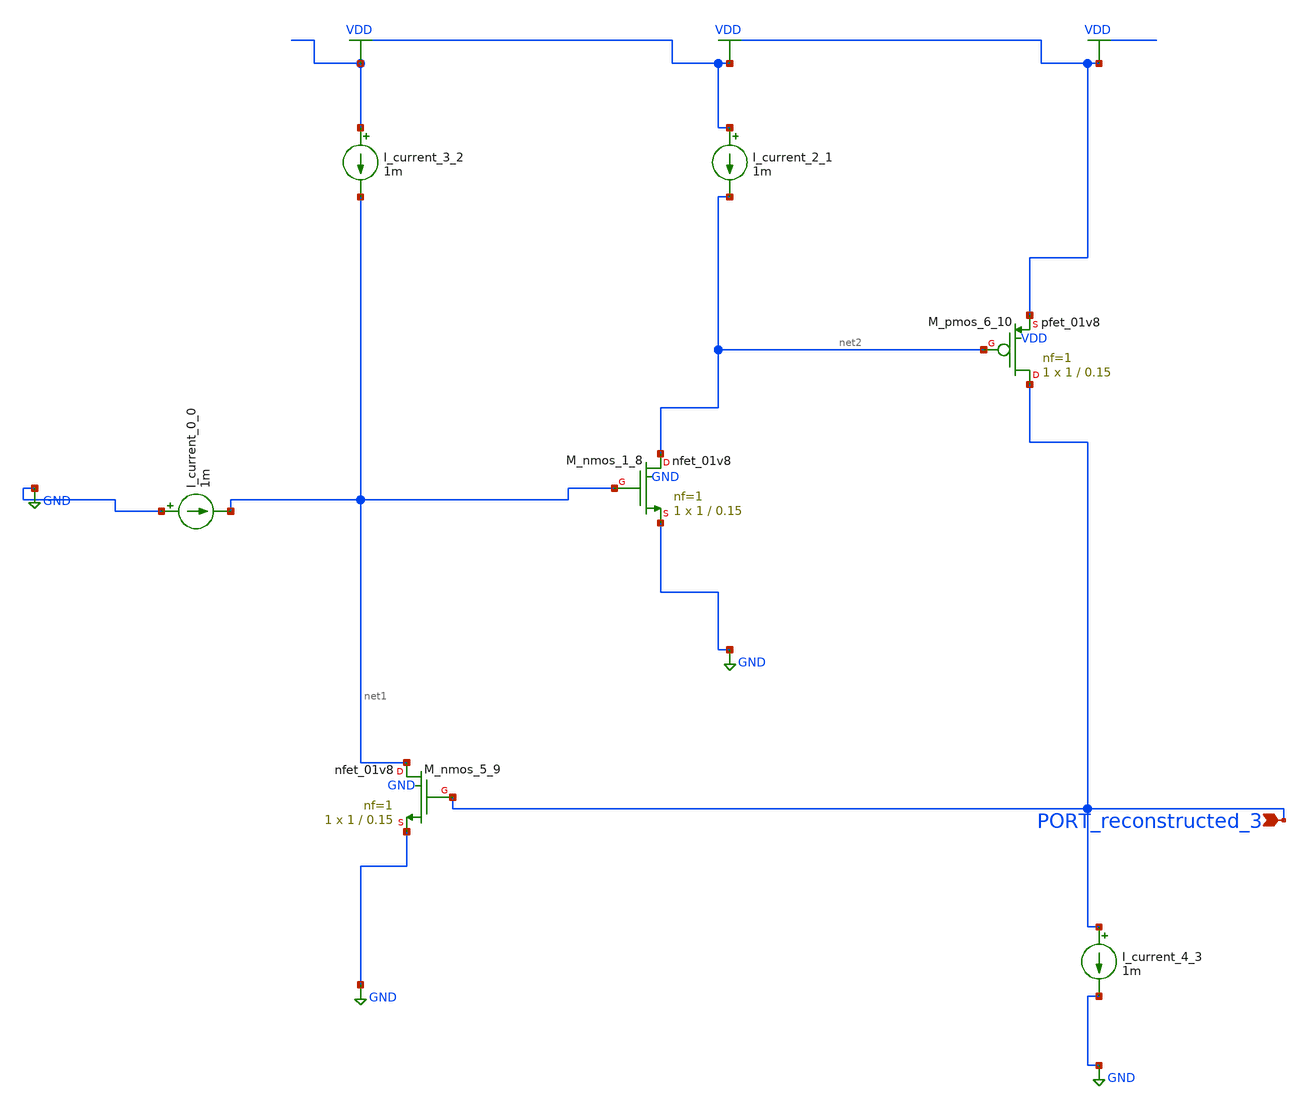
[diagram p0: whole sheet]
** sch_path: schematics/AMSNet/743.sch
**.subckt 743 PORT_reconstructed_3
*.ipin PORT_reconstructed_3
I_current_0_0 GND net1 1m
I_current_2_1 VDD net2 1m
I_current_3_2 VDD net1 1m
I_current_4_3 PORT_reconstructed_3 GND 1m
XM_nmos_1_8 net2 net1 GND GND sky130_fd_pr__nfet_01v8 L=0.15 W=1 nf=1 ad='int((1 + 1)/2) * 1 / 1 * 0.29'
+ as='int((1 + 2)/2) * 1 / 1 * 0.29' pd='2*int((1 + 1)/2) * (1 / 1 + 0.29)' ps='2*int((1 + 2)/2) * (1 / 1 + 0.29)'
+ nrd='0.29 / 1 ' nrs='0.29 / 1 ' sa=0 sb=0 sd=0 mult=1 m=1
XM_nmos_5_9 net1 PORT_reconstructed_3 GND GND sky130_fd_pr__nfet_01v8 L=0.15 W=1 nf=1 ad='int((1 + 1)/2) * 1 / 1 * 0.29'
+ as='int((1 + 2)/2) * 1 / 1 * 0.29' pd='2*int((1 + 1)/2) * (1 / 1 + 0.29)' ps='2*int((1 + 2)/2) * (1 / 1 + 0.29)'
+ nrd='0.29 / 1 ' nrs='0.29 / 1 ' sa=0 sb=0 sd=0 mult=1 m=1
XM_pmos_6_10 PORT_reconstructed_3 net2 VDD VDD sky130_fd_pr__pfet_01v8 L=0.15 W=1 nf=1 ad='int((1 + 1)/2) * 1 / 1 * 0.29'
+ as='int((1 + 2)/2) * 1 / 1 * 0.29' pd='2*int((1 + 1)/2) * (1 / 1 + 0.29)' ps='2*int((1 + 2)/2) * (1 / 1 + 0.29)'
+ nrd='0.29 / 1 ' nrs='0.29 / 1 ' sa=0 sb=0 sd=0 mult=1 m=1
**.ends
.GLOBAL GND
.GLOBAL VDD
.end
